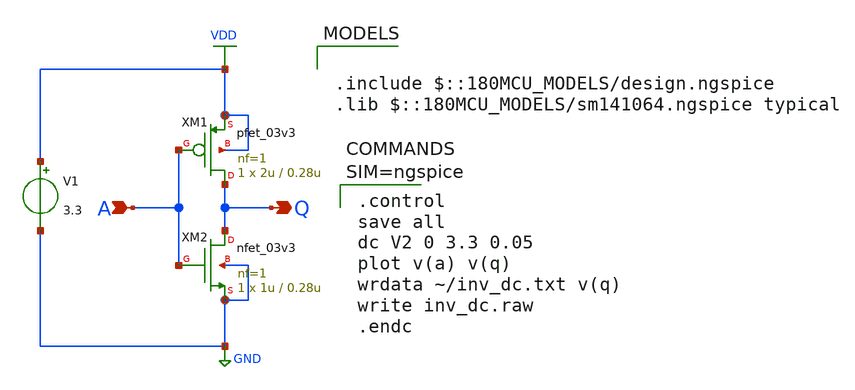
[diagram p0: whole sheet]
** sch_path: inv_dc.sch
**.subckt inv_dc Q A
*.opin Q
*.ipin A
XM1 Q A VDD VDD pfet_03v3 L=0.28u W=2u nf=1 ad='int((nf+1)/2) * W/nf * 0.18u' as='int((nf+2)/2) * W/nf * 0.18u'
+ pd='2*int((nf+1)/2) * (W/nf + 0.18u)' ps='2*int((nf+2)/2) * (W/nf + 0.18u)' nrd='0.18u / W' nrs='0.18u / W'
+ sa=0 sb=0 sd=0 m=1
XM2 Q A GND GND nfet_03v3 L=0.28u W=1u nf=1 ad='int((nf+1)/2) * W/nf * 0.18u' as='int((nf+2)/2) * W/nf * 0.18u'
+ pd='2*int((nf+1)/2) * (W/nf + 0.18u)' ps='2*int((nf+2)/2) * (W/nf + 0.18u)' nrd='0.18u / W' nrs='0.18u / W'
+ sa=0 sb=0 sd=0 m=1
V1 VDD GND 3.3
**** begin user architecture code

.include $::180MCU_MODELS/design.ngspice
.lib $::180MCU_MODELS/sm141064.ngspice typical



.control
save all
dc V2 0 3.3 0.05
plot v(a) v(q)
wrdata ~/inv_dc.txt v(q)
write inv_dc.raw
.endc



**** end user architecture code
**.ends
.GLOBAL VDD
.GLOBAL GND
.end
